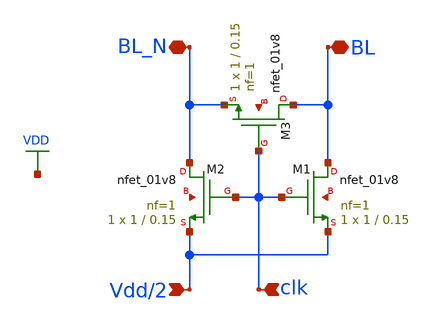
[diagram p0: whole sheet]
** sch_path: analog/schematics/SRAM_precharge.sch
**.subckt SRAM_precharge BL BL_N Vdd/2 clk
*.iopin BL
*.iopin BL_N
*.ipin Vdd/2
*.ipin clk
XM1 BL clk Vdd/2 net1 sky130_fd_pr__nfet_01v8 L=0.15 W=1 nf=1 ad='int((nf+1)/2) * W/nf * 0.29' as='int((nf+2)/2) * W/nf * 0.29'
+ pd='2*int((nf+1)/2) * (W/nf + 0.29)' ps='2*int((nf+2)/2) * (W/nf + 0.29)' nrd='0.29 / W' nrs='0.29 / W'
+ sa=0 sb=0 sd=0 mult=1 m=1
XM2 BL_N clk Vdd/2 net2 sky130_fd_pr__nfet_01v8 L=0.15 W=1 nf=1 ad='int((nf+1)/2) * W/nf * 0.29' as='int((nf+2)/2) * W/nf * 0.29'
+ pd='2*int((nf+1)/2) * (W/nf + 0.29)' ps='2*int((nf+2)/2) * (W/nf + 0.29)' nrd='0.29 / W' nrs='0.29 / W'
+ sa=0 sb=0 sd=0 mult=1 m=1
XM3 BL clk BL_N net3 sky130_fd_pr__nfet_01v8 L=0.15 W=1 nf=1 ad='int((nf+1)/2) * W/nf * 0.29' as='int((nf+2)/2) * W/nf * 0.29'
+ pd='2*int((nf+1)/2) * (W/nf + 0.29)' ps='2*int((nf+2)/2) * (W/nf + 0.29)' nrd='0.29 / W' nrs='0.29 / W'
+ sa=0 sb=0 sd=0 mult=1 m=1
**.ends
.GLOBAL VDD
.end
